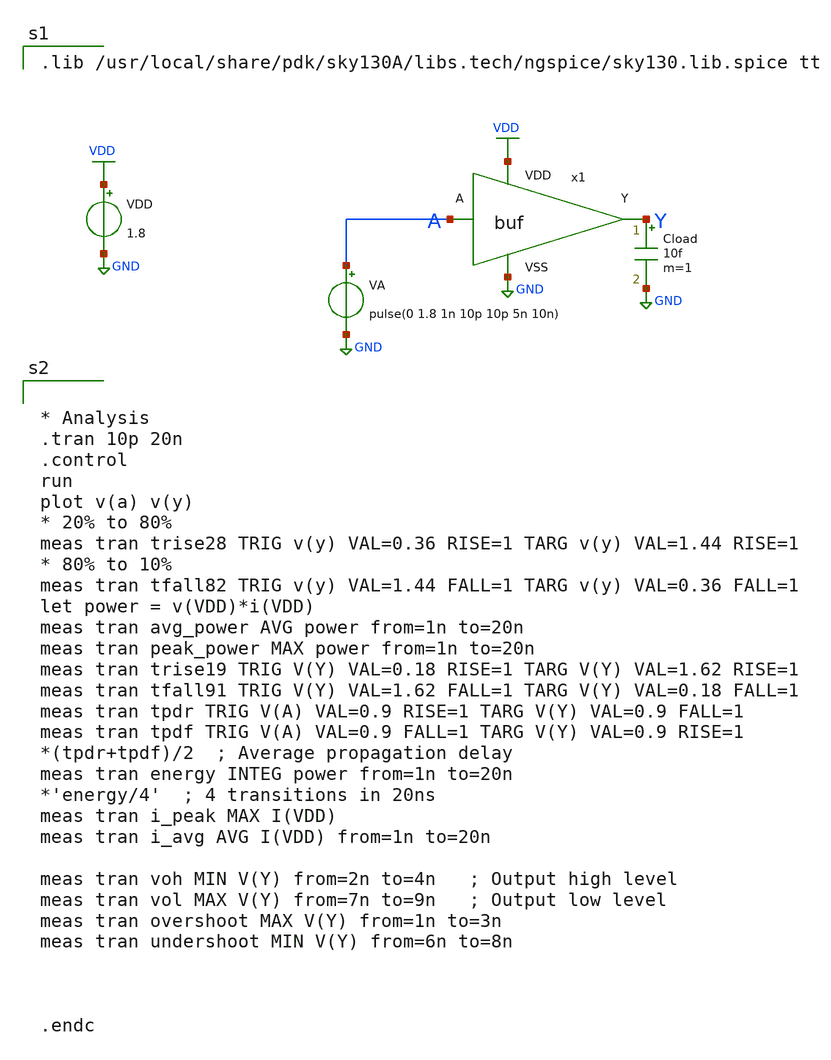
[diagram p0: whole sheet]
** sch_path: buffer/design_circuit/tb_buf.sch
**.subckt tb_buf
x1 A Y VDD GND buf
Cload Y GND 10f m=1
VDD VDD GND 1.8
VA A GND pulse(0 1.8 1n 10p 10p 5n 10n)
**** begin user architecture code

.lib /usr/local/share/pdk/sky130A/libs.tech/ngspice/sky130.lib.spice tt



* Analysis
.tran 10p 20n
.control
run
plot v(a) v(y)
* 20% to 80%
meas tran trise28 TRIG v(y) VAL=0.36 RISE=1 TARG v(y) VAL=1.44 RISE=1
* 80% to 10%
meas tran tfall82 TRIG v(y) VAL=1.44 FALL=1 TARG v(y) VAL=0.36 FALL=1
let power = v(VDD)*i(VDD)
meas tran avg_power AVG power from=1n to=20n
meas tran peak_power MAX power from=1n to=20n
meas tran trise19 TRIG V(Y) VAL=0.18 RISE=1 TARG V(Y) VAL=1.62 RISE=1
meas tran tfall91 TRIG V(Y) VAL=1.62 FALL=1 TARG V(Y) VAL=0.18 FALL=1
meas tran tpdr TRIG V(A) VAL=0.9 RISE=1 TARG V(Y) VAL=0.9 FALL=1
meas tran tpdf TRIG V(A) VAL=0.9 FALL=1 TARG V(Y) VAL=0.9 RISE=1
*(tpdr+tpdf)/2  ; Average propagation delay
meas tran energy INTEG power from=1n to=20n
*'energy/4'  ; 4 transitions in 20ns
meas tran i_peak MAX I(VDD)
meas tran i_avg AVG I(VDD) from=1n to=20n

meas tran voh MIN V(Y) from=2n to=4n   ; Output high level
meas tran vol MAX V(Y) from=7n to=9n   ; Output low level
meas tran overshoot MAX V(Y) from=1n to=3n
meas tran undershoot MIN V(Y) from=6n to=8n



.endc


**** end user architecture code
**.ends

* expanding   symbol:  buf.sym # of pins=4
** sym_path: buffer/design_circuit/buf.sym
** sch_path: buffer/design_circuit/buf.sch
.subckt buf A Y VDD VSS
*.ipin A
*.opin Y
*.ipin VDD
*.ipin VSS
x1 A net1 VDD VSS invx1
x2 net1 Y VDD VSS invx2
.ends


* expanding   symbol:  invx1.sym # of pins=4
** sym_path: buffer/design_circuit/invx1.sym
** sch_path: buffer/design_circuit/invx1.sch
.subckt invx1 A Y VDD VSS
*.ipin A
*.opin Y
*.ipin VDD
*.ipin VSS
XM1 Y A VDD VDD sky130_fd_pr__pfet_01v8 L=0.15 W=1 nf=1 ad='int((nf+1)/2) * W/nf * 0.29' as='int((nf+2)/2) * W/nf * 0.29'
+ pd='2*int((nf+1)/2) * (W/nf + 0.29)' ps='2*int((nf+2)/2) * (W/nf + 0.29)' nrd='0.29 / W' nrs='0.29 / W'
+ sa=0 sb=0 sd=0 mult=1 m=1
XM2 Y A VSS VSS sky130_fd_pr__nfet_01v8 L=0.15 W=0.42 nf=1 ad='int((nf+1)/2) * W/nf * 0.29' as='int((nf+2)/2) * W/nf * 0.29'
+ pd='2*int((nf+1)/2) * (W/nf + 0.29)' ps='2*int((nf+2)/2) * (W/nf + 0.29)' nrd='0.29 / W' nrs='0.29 / W'
+ sa=0 sb=0 sd=0 mult=1 m=1
.ends


* expanding   symbol:  invx2.sym # of pins=4
** sym_path: buffer/design_circuit/invx2.sym
** sch_path: buffer/design_circuit/invx2.sch
.subckt invx2 A Y VDD VSS
*.ipin A
*.opin Y
*.ipin VDD
*.ipin VSS
XM1 Y A VDD VDD sky130_fd_pr__pfet_01v8 L=0.15 W=2 nf=1 ad='int((nf+1)/2) * W/nf * 0.29' as='int((nf+2)/2) * W/nf * 0.29'
+ pd='2*int((nf+1)/2) * (W/nf + 0.29)' ps='2*int((nf+2)/2) * (W/nf + 0.29)' nrd='0.29 / W' nrs='0.29 / W'
+ sa=0 sb=0 sd=0 mult=1 m=1
XM2 Y A VSS VSS sky130_fd_pr__nfet_01v8 L=0.15 W=0.84 nf=1 ad='int((nf+1)/2) * W/nf * 0.29' as='int((nf+2)/2) * W/nf * 0.29'
+ pd='2*int((nf+1)/2) * (W/nf + 0.29)' ps='2*int((nf+2)/2) * (W/nf + 0.29)' nrd='0.29 / W' nrs='0.29 / W'
+ sa=0 sb=0 sd=0 mult=1 m=1
.ends

.GLOBAL GND
.GLOBAL VDD
.end
